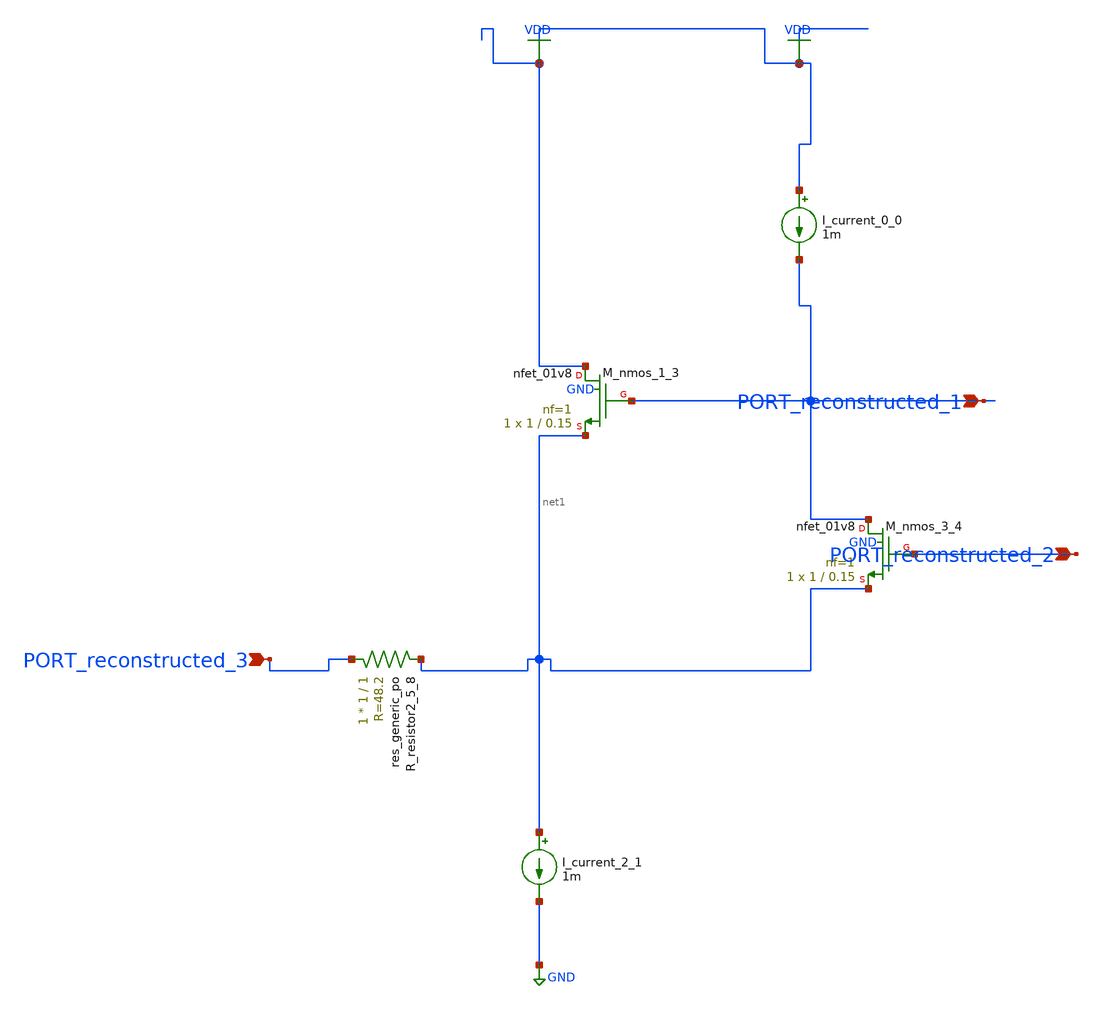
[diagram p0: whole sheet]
** sch_path: schematics/AMSNet/416.sch
**.subckt 416 PORT_reconstructed_2 PORT_reconstructed_1 PORT_reconstructed_3
*.ipin PORT_reconstructed_2
*.ipin PORT_reconstructed_1
*.ipin PORT_reconstructed_3
I_current_0_0 VDD PORT_reconstructed_1 1m
I_current_2_1 net1 GND 1m
XM_nmos_1_3 VDD PORT_reconstructed_1 net1 GND sky130_fd_pr__nfet_01v8 L=0.15 W=1 nf=1 ad='int((1 + 1)/2) * 1 / 1 * 0.29'
+ as='int((1 + 2)/2) * 1 / 1 * 0.29' pd='2*int((1 + 1)/2) * (1 / 1 + 0.29)' ps='2*int((1 + 2)/2) * (1 / 1 + 0.29)'
+ nrd='0.29 / 1 ' nrs='0.29 / 1 ' sa=0 sb=0 sd=0 mult=1 m=1
XM_nmos_3_4 PORT_reconstructed_1 PORT_reconstructed_2 net1 GND sky130_fd_pr__nfet_01v8 L=0.15 W=1 nf=1
+ ad='int((1 + 1)/2) * 1 / 1 * 0.29' as='int((1 + 2)/2) * 1 / 1 * 0.29' pd='2*int((1 + 1)/2) * (1 / 1 + 0.29)'
+ ps='2*int((1 + 2)/2) * (1 / 1 + 0.29)' nrd='0.29 / 1 ' nrs='0.29 / 1 ' sa=0 sb=0 sd=0 mult=1 m=1
XR_resistor2_5_8 PORT_reconstructed_3 net1 sky130_fd_pr__res_generic_po W=1 L=1 m=1
**.ends
.GLOBAL GND
.GLOBAL VDD
.end
